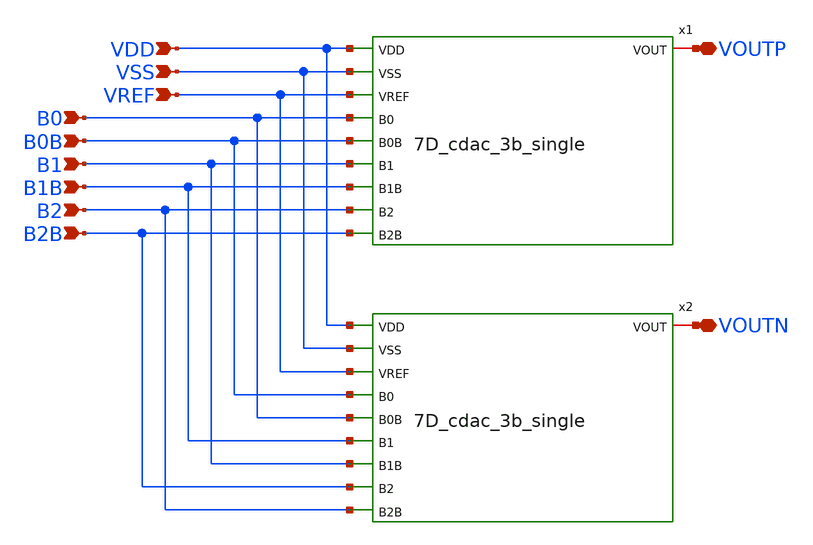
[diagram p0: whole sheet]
** sch_path: designs/libs/core_matchmaker/7D_cdac_3b_diff/7D_cdac_3b_diff.sch
**.subckt 7D_cdac_3b_diff VOUTP VOUTN VDD VSS VREF B0 B0B B1 B1B B2 B2B
*.iopin VOUTP
*.iopin VOUTN
*.ipin VDD
*.ipin VSS
*.ipin VREF
*.ipin B0
*.ipin B0B
*.ipin B1
*.ipin B1B
*.ipin B2
*.ipin B2B
x1 VDD VSS VREF B0 B0B B1 B1B B2 B2B VOUTP 7D_cdac_3b_single
x2 VDD VSS VREF B0B B0 B1B B1 B2B B2 VOUTN 7D_cdac_3b_single
**.ends
.end
